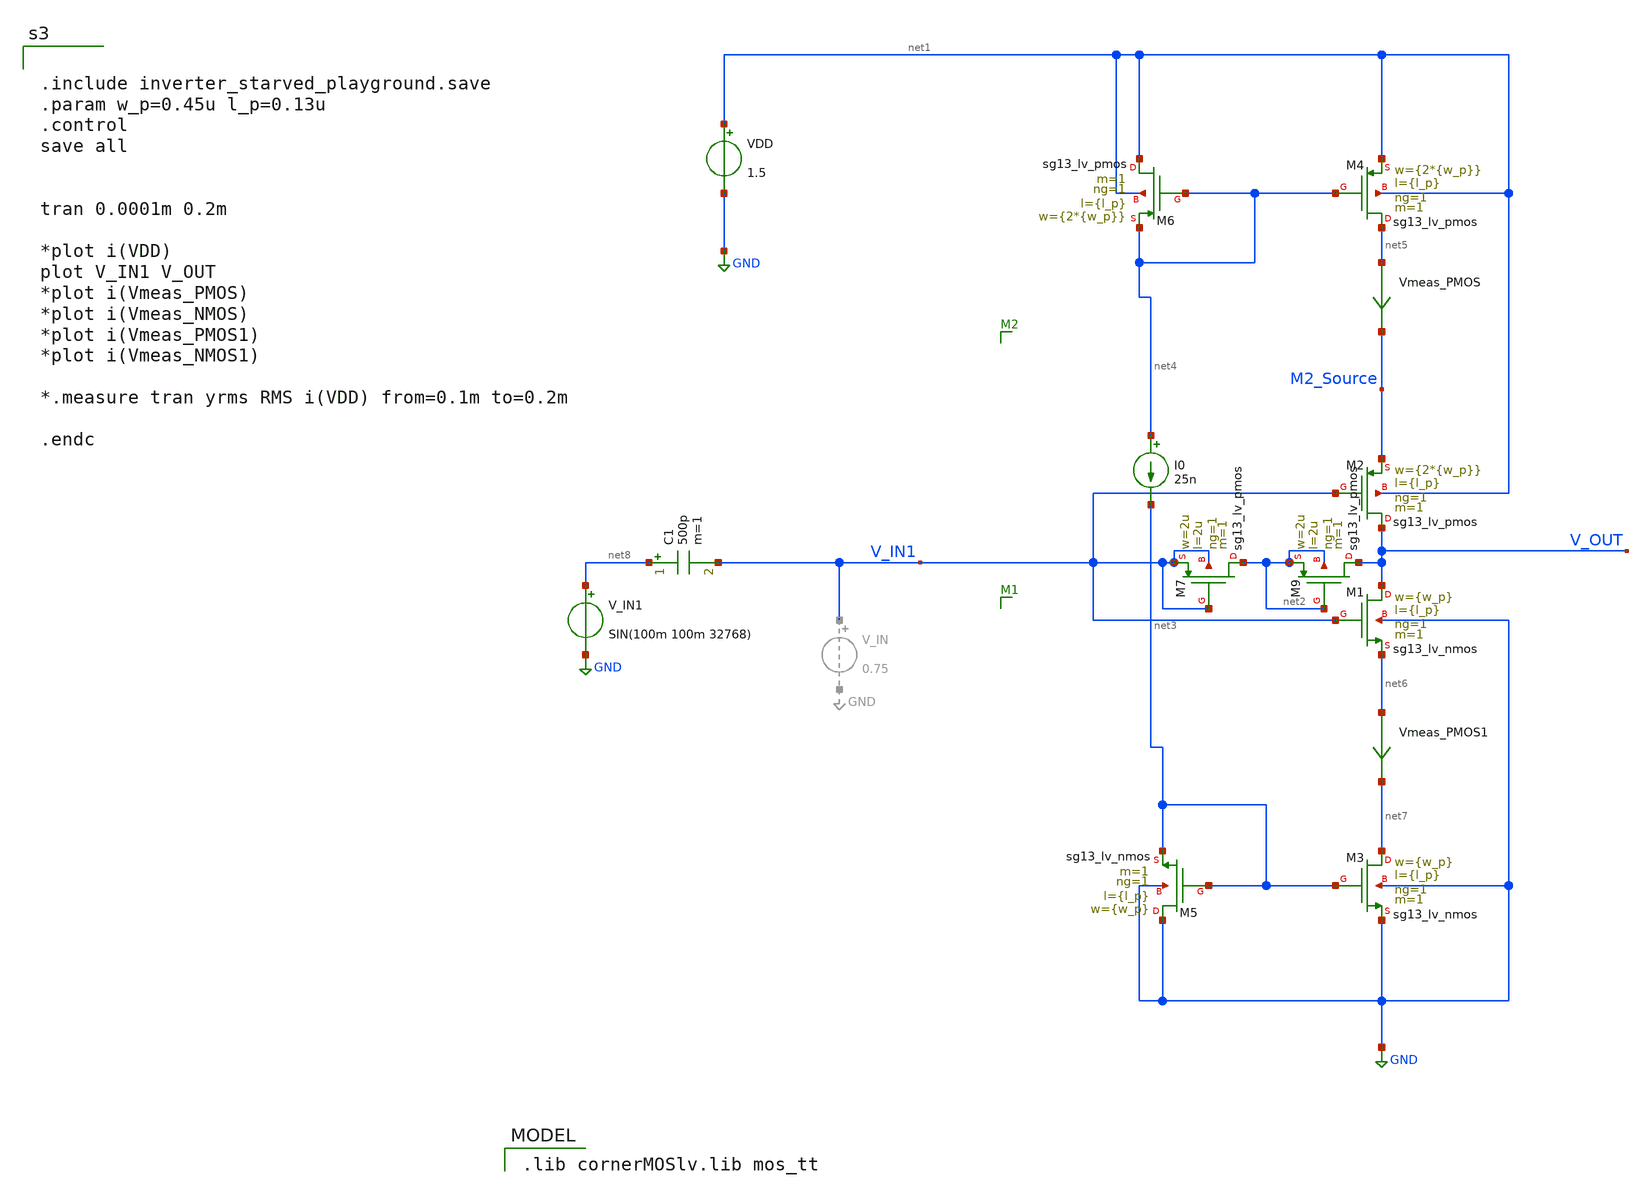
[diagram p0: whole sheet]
** sch_path: inverter_starved_playground.sch
**.subckt inverter_starved_playground
XM1 V_OUT V_IN1 net6 GND sg13_lv_nmos w={w_p} l={l_p} ng=1 m=1 mm_ok=1
XM2 V_OUT V_IN1 M2_Source net1 sg13_lv_pmos w={2*{w_p}} l={l_p} ng=1 m=1 mm_ok=1
VDD net1 GND 1.5
XM3 net7 net3 GND GND sg13_lv_nmos w={w_p} l={l_p} ng=1 m=1 mm_ok=1
XM4 net5 net4 net1 net1 sg13_lv_pmos w={2*{w_p}} l={l_p} ng=1 m=1 mm_ok=1
XM5 GND net3 net3 GND sg13_lv_nmos w={w_p} l={l_p} ng=1 m=1 mm_ok=1
XM6 net1 net4 net4 net1 sg13_lv_pmos w={2*{w_p}} l={l_p} ng=1 m=1 mm_ok=1
I0 net4 net3 25n
Vmeas_PMOS net5 M2_Source 0
.save i(vmeas_pmos)
Vmeas_PMOS1 net6 net7 0
.save i(vmeas_pmos1)
V_IN1 net8 GND SIN(100m 100m 32768)
C1 net8 V_IN1 500p m=1
XM9 V_OUT net2 net2 net2 sg13_lv_pmos w=2u l=2u ng=1 m=1 mm_ok=1
XM7 net2 V_IN1 V_IN1 V_IN1 sg13_lv_pmos w=2u l=2u ng=1 m=1 mm_ok=1
**** begin user architecture code
 .lib cornerMOSlv.lib mos_tt



.include inverter_starved_playground.save
.param w_p=0.45u l_p=0.13u
.control
save all


tran 0.0001m 0.2m

*plot i(VDD)
plot V_IN1 V_OUT
*plot i(Vmeas_PMOS)
*plot i(Vmeas_NMOS)
*plot i(Vmeas_PMOS1)
*plot i(Vmeas_NMOS1)

*.measure tran yrms RMS i(VDD) from=0.1m to=0.2m

.endc


**** end user architecture code
**.ends
.GLOBAL GND
.end
